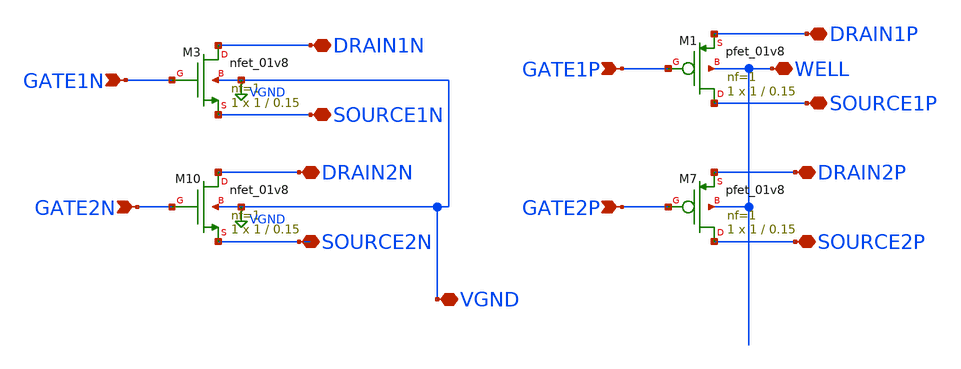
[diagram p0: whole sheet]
** sch_path: libs.ref/sky130_hilas_sc/xschem/sky130_hilas_Trans2med.sch
**.subckt sky130_hilas_Trans2med GATE2N WELL SOURCE2P GATE1N DRAIN1N DRAIN2N GATE2P SOURCE1P GATE1P
*+ DRAIN1P DRAIN2P SOURCE2N SOURCE1N VGND
*.ipin GATE2N
*.iopin WELL
*.iopin SOURCE2P
*.ipin GATE1N
*.iopin DRAIN1N
*.iopin DRAIN2N
*.ipin GATE2P
*.iopin SOURCE1P
*.ipin GATE1P
*.iopin DRAIN1P
*.iopin DRAIN2P
*.iopin SOURCE2N
*.iopin SOURCE1N
*.iopin VGND
XM1 SOURCE1P GATE1P DRAIN1P WELL sky130_fd_pr__pfet_01v8 L=0.15 W=1 nf=1 ad='int((nf+1)/2) * W/nf * 0.29'
+ as='int((nf+2)/2) * W/nf * 0.29' pd='2*int((nf+1)/2) * (W/nf + 0.29)' ps='2*int((nf+2)/2) * (W/nf + 0.29)'
+ nrd='0.29 / W' nrs='0.29 / W' sa=0 sb=0 sd=0 mult=1 m=1
XM3 DRAIN1N GATE1N SOURCE1N VGND sky130_fd_pr__nfet_01v8 L=0.15 W=1 nf=1 ad='int((nf+1)/2) * W/nf * 0.29'
+ as='int((nf+2)/2) * W/nf * 0.29' pd='2*int((nf+1)/2) * (W/nf + 0.29)' ps='2*int((nf+2)/2) * (W/nf + 0.29)'
+ nrd='0.29 / W' nrs='0.29 / W' sa=0 sb=0 sd=0 mult=1 m=1
XM7 SOURCE2P GATE2P DRAIN2P WELL sky130_fd_pr__pfet_01v8 L=0.15 W=1 nf=1 ad='int((nf+1)/2) * W/nf * 0.29'
+ as='int((nf+2)/2) * W/nf * 0.29' pd='2*int((nf+1)/2) * (W/nf + 0.29)' ps='2*int((nf+2)/2) * (W/nf + 0.29)'
+ nrd='0.29 / W' nrs='0.29 / W' sa=0 sb=0 sd=0 mult=1 m=1
XM10 DRAIN2N GATE2N SOURCE2N VGND sky130_fd_pr__nfet_01v8 L=0.15 W=1 nf=1 ad='int((nf+1)/2) * W/nf * 0.29'
+ as='int((nf+2)/2) * W/nf * 0.29' pd='2*int((nf+1)/2) * (W/nf + 0.29)' ps='2*int((nf+2)/2) * (W/nf + 0.29)'
+ nrd='0.29 / W' nrs='0.29 / W' sa=0 sb=0 sd=0 mult=1 m=1
**.ends
.GLOBAL VGND
.end
